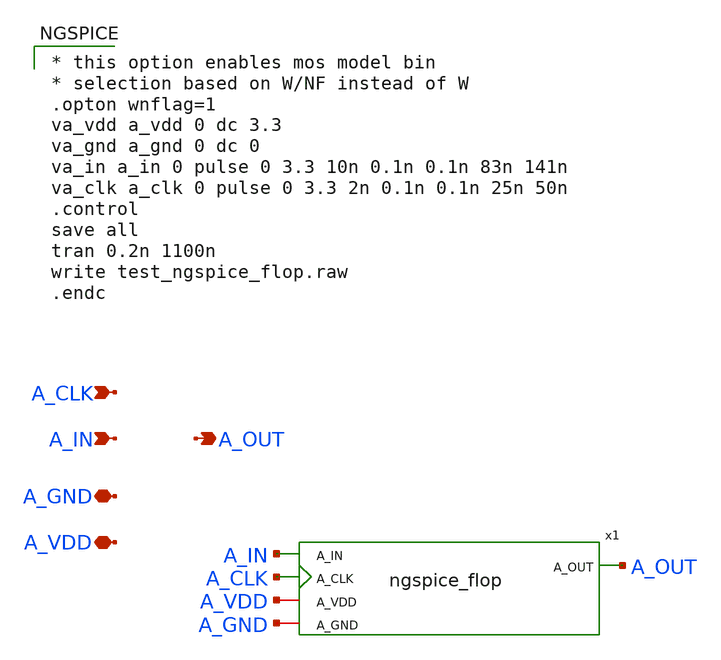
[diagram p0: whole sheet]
** sch_path: xschem/test_ngspice_flop.sch
**.subckt test_ngspice_flop A_VDD A_IN A_GND A_CLK A_OUT
*.iopin A_VDD
*.ipin A_IN
*.iopin A_GND
*.ipin A_CLK
*.opin A_OUT
x1 A_OUT A_IN A_CLK A_GND A_VDD ngspice_flop
**** begin user architecture code

* this option enables mos model bin
* selection based on W/NF instead of W
.opton wnflag=1
va_vdd a_vdd 0 dc 3.3
va_gnd a_gnd 0 dc 0
va_in a_in 0 pulse 0 3.3 10n 0.1n 0.1n 83n 141n
va_clk a_clk 0 pulse 0 3.3 2n 0.1n 0.1n 25n 50n
.control
save all
tran 0.2n 1100n
write test_ngspice_flop.raw
.endc


**** end user architecture code
**.ends

* expanding   symbol:  /foss/designs/TO202406_CMOSVCO_Esm22/xschem/ngspice_flop.sym # of pins=5
** sym_path: /foss/designs/TO202406_CMOSVCO_Esm22/xschem/ngspice_flop.sym
** sch_path: /foss/designs/TO202406_CMOSVCO_Esm22/xschem/ngspice_flop.sch
.subckt ngspice_flop A_OUT A_IN A_CLK A_GND A_VDD
*.iopin A_VDD
*.ipin A_IN
*.opin A_OUT
*.ipin A_CLK
*.iopin A_GND
* noconn A_VDD
* noconn A_IN
* noconn A_CLK
* noconn A_GND
* noconn A_OUT
**** begin user architecture code
.model todig_3v3 adc_bridge(in_high=2.2 in_low=1.1  rise_delay=10n fall_delay=10n)
.model toana_3v3 dac_bridge(out_high=3.3 out_low=0)
.model ddflop d_dff(ic=0 rise_delay=1n fall_delay=1n)
AA2D1 [A_GND] [d_gnd] todig_3v3
AA2D2 [A_IN] [d_in] todig_3v3
AA2D3 [A_CLK] [d_clk] todig_3v3
A1 d_in d_clk d_gnd d_gnd d_out NULL ddflop
AD2A1 [d_out] [A_OUT] toana_3v3

**** end user architecture code
.ends

.end
